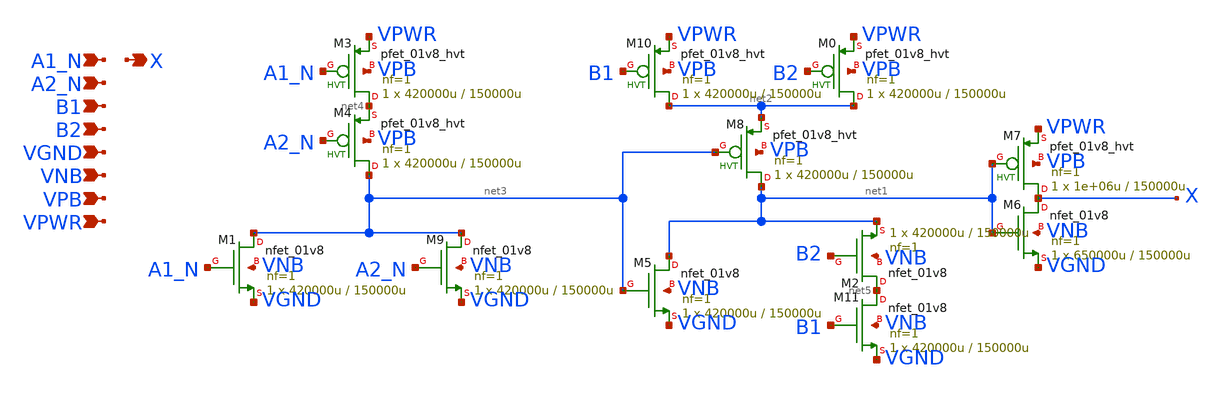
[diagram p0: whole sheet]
** sch_path: schematics/a2bb2o/sky130_fd_sc_hd__a2bb2o_1.sch
**.subckt sky130_fd_sc_hd__a2bb2o_1 A1_N A2_N B1 B2 VGND VNB VPB VPWR X
*.ipin A1_N
*.ipin A2_N
*.ipin B1
*.ipin B2
*.ipin VGND
*.ipin VNB
*.ipin VPB
*.ipin VPWR
*.opin X
XM7 X net1 VPWR VPB sky130_fd_pr__pfet_01v8_hvt L=150000u W=1e+06u nf=1 ad='int((1 + 1)/2) * 1e+06u / 1 * 0.29'
+ as='int((1 + 2)/2) * 1e+06u / 1 * 0.29' pd='2*int((1 + 1)/2) * (1e+06u / 1 + 0.29)' ps='2*int((1 + 2)/2) * (1e+06u / 1 + 0.29)'
+ nrd='0.29 / 1e+06u ' nrs='0.29 / 1e+06u ' sa=0 sb=0 sd=0 mult=1 m=1
XM6 X net1 VGND VNB sky130_fd_pr__nfet_01v8 L=150000u W=650000u nf=1 ad='int((1 + 1)/2) * 650000u / 1 * 0.29'
+ as='int((1 + 2)/2) * 650000u / 1 * 0.29' pd='2*int((1 + 1)/2) * (650000u / 1 + 0.29)' ps='2*int((1 + 2)/2) * (650000u / 1 + 0.29)'
+ nrd='0.29 / 650000u ' nrs='0.29 / 650000u ' sa=0 sb=0 sd=0 mult=1 m=1
XM3 net4 A1_N VPWR VPB sky130_fd_pr__pfet_01v8_hvt L=150000u W=420000u nf=1 ad='int((1 + 1)/2) * 420000u / 1 * 0.29'
+ as='int((1 + 2)/2) * 420000u / 1 * 0.29' pd='2*int((1 + 1)/2) * (420000u / 1 + 0.29)' ps='2*int((1 + 2)/2) * (420000u / 1 + 0.29)'
+ nrd='0.29 / 420000u ' nrs='0.29 / 420000u ' sa=0 sb=0 sd=0 mult=1 m=1
XM4 net3 A2_N net4 VPB sky130_fd_pr__pfet_01v8_hvt L=150000u W=420000u nf=1 ad='int((1 + 1)/2) * 420000u / 1 * 0.29'
+ as='int((1 + 2)/2) * 420000u / 1 * 0.29' pd='2*int((1 + 1)/2) * (420000u / 1 + 0.29)' ps='2*int((1 + 2)/2) * (420000u / 1 + 0.29)'
+ nrd='0.29 / 420000u ' nrs='0.29 / 420000u ' sa=0 sb=0 sd=0 mult=1 m=1
XM8 net1 net3 net2 VPB sky130_fd_pr__pfet_01v8_hvt L=150000u W=420000u nf=1 ad='int((1 + 1)/2) * 420000u / 1 * 0.29'
+ as='int((1 + 2)/2) * 420000u / 1 * 0.29' pd='2*int((1 + 1)/2) * (420000u / 1 + 0.29)' ps='2*int((1 + 2)/2) * (420000u / 1 + 0.29)'
+ nrd='0.29 / 420000u ' nrs='0.29 / 420000u ' sa=0 sb=0 sd=0 mult=1 m=1
XM10 net2 B1 VPWR VPB sky130_fd_pr__pfet_01v8_hvt L=150000u W=420000u nf=1 ad='int((1 + 1)/2) * 420000u / 1 * 0.29'
+ as='int((1 + 2)/2) * 420000u / 1 * 0.29' pd='2*int((1 + 1)/2) * (420000u / 1 + 0.29)' ps='2*int((1 + 2)/2) * (420000u / 1 + 0.29)'
+ nrd='0.29 / 420000u ' nrs='0.29 / 420000u ' sa=0 sb=0 sd=0 mult=1 m=1
XM0 net2 B2 VPWR VPB sky130_fd_pr__pfet_01v8_hvt L=150000u W=420000u nf=1 ad='int((1 + 1)/2) * 420000u / 1 * 0.29'
+ as='int((1 + 2)/2) * 420000u / 1 * 0.29' pd='2*int((1 + 1)/2) * (420000u / 1 + 0.29)' ps='2*int((1 + 2)/2) * (420000u / 1 + 0.29)'
+ nrd='0.29 / 420000u ' nrs='0.29 / 420000u ' sa=0 sb=0 sd=0 mult=1 m=1
XM1 net3 A1_N VGND VNB sky130_fd_pr__nfet_01v8 L=150000u W=420000u nf=1 ad='int((1 + 1)/2) * 420000u / 1 * 0.29'
+ as='int((1 + 2)/2) * 420000u / 1 * 0.29' pd='2*int((1 + 1)/2) * (420000u / 1 + 0.29)' ps='2*int((1 + 2)/2) * (420000u / 1 + 0.29)'
+ nrd='0.29 / 420000u ' nrs='0.29 / 420000u ' sa=0 sb=0 sd=0 mult=1 m=1
XM9 net3 A2_N VGND VNB sky130_fd_pr__nfet_01v8 L=150000u W=420000u nf=1 ad='int((1 + 1)/2) * 420000u / 1 * 0.29'
+ as='int((1 + 2)/2) * 420000u / 1 * 0.29' pd='2*int((1 + 1)/2) * (420000u / 1 + 0.29)' ps='2*int((1 + 2)/2) * (420000u / 1 + 0.29)'
+ nrd='0.29 / 420000u ' nrs='0.29 / 420000u ' sa=0 sb=0 sd=0 mult=1 m=1
XM5 net1 net3 VGND VNB sky130_fd_pr__nfet_01v8 L=150000u W=420000u nf=1 ad='int((1 + 1)/2) * 420000u / 1 * 0.29'
+ as='int((1 + 2)/2) * 420000u / 1 * 0.29' pd='2*int((1 + 1)/2) * (420000u / 1 + 0.29)' ps='2*int((1 + 2)/2) * (420000u / 1 + 0.29)'
+ nrd='0.29 / 420000u ' nrs='0.29 / 420000u ' sa=0 sb=0 sd=0 mult=1 m=1
XM11 net5 B1 VGND VNB sky130_fd_pr__nfet_01v8 L=150000u W=420000u nf=1 ad='int((1 + 1)/2) * 420000u / 1 * 0.29'
+ as='int((1 + 2)/2) * 420000u / 1 * 0.29' pd='2*int((1 + 1)/2) * (420000u / 1 + 0.29)' ps='2*int((1 + 2)/2) * (420000u / 1 + 0.29)'
+ nrd='0.29 / 420000u ' nrs='0.29 / 420000u ' sa=0 sb=0 sd=0 mult=1 m=1
XM2 net5 B2 net1 VNB sky130_fd_pr__nfet_01v8 L=150000u W=420000u nf=1 ad='int((1 + 1)/2) * 420000u / 1 * 0.29'
+ as='int((1 + 2)/2) * 420000u / 1 * 0.29' pd='2*int((1 + 1)/2) * (420000u / 1 + 0.29)' ps='2*int((1 + 2)/2) * (420000u / 1 + 0.29)'
+ nrd='0.29 / 420000u ' nrs='0.29 / 420000u ' sa=0 sb=0 sd=0 mult=1 m=1
**.ends
.end
